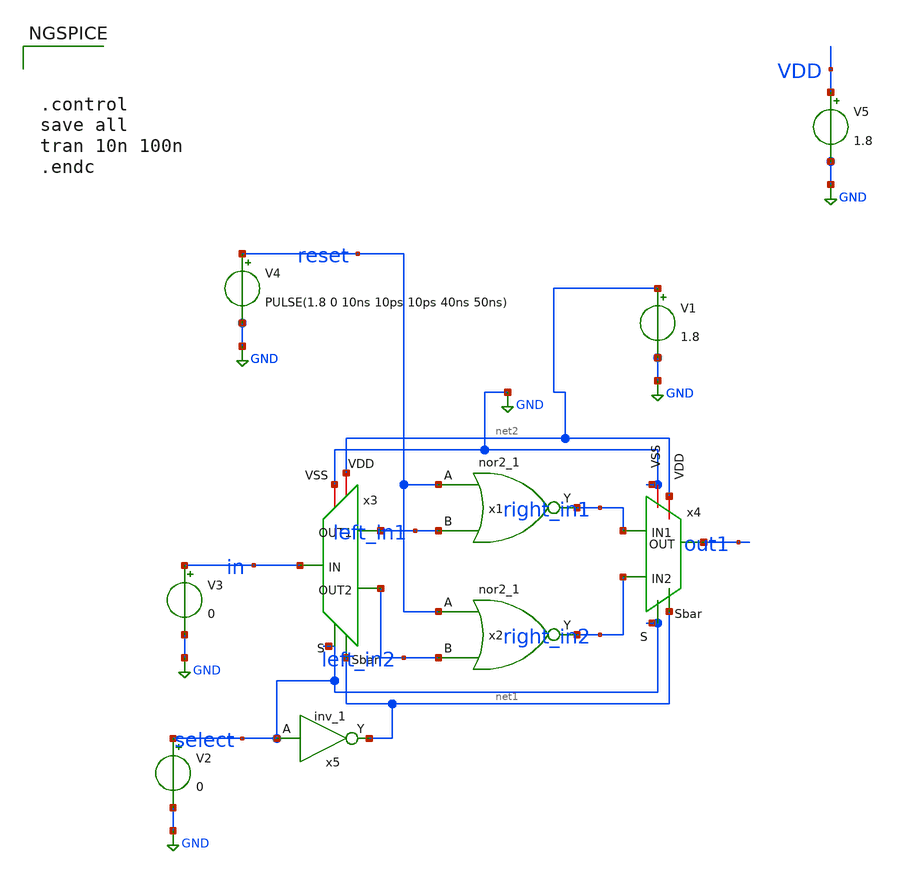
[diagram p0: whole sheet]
** sch_path: xiaolin/singlestage_tb.sch
**.subckt singlestage_tb
x1 reset left_in1 GND GND VDD VDD right_in1 sky130_fd_sc_hd__nor2_1
x2 reset left_in2 GND GND VDD VDD right_in2 sky130_fd_sc_hd__nor2_1
x3 select GND left_in1 net2 in net1 left_in2 demux2-1
x4 select GND right_in1 net2 out1 net1 right_in2 mux2-1
x5 select GND GND VDD VDD net1 sky130_fd_sc_hd__inv_1
V1 net2 GND 1.8
V2 select GND 0
V3 in GND 0
V4 reset GND PULSE(1.8 0 10ns 10ps 10ps 40ns 50ns)
V5 VDD GND 1.8
**** begin user architecture code

** opencircuitdesign pdks install
*.lib /farmshare/home/classes/ee/372/PDKs/open_pdks/sky130/sky130A/libs.tech/ngspice/sky130.lib.spice mc
.lib ~/372puf/ee372/sky130A/libs.tech/ngspice/sky130.lib.spice mc
.include /farmshare/home/classes/ee/372/PDKs/open_pdks/sky130/sky130A/libs.ref/sky130_fd_sc_hd/spice/sky130_fd_sc_hd.spice






.control
save all
tran 10n 100n
.endc


**** end user architecture code
**.ends

* expanding   symbol:  demux2-1.sym # of pins=7
** sym_path: xiaolin/demux2-1.sym
** sch_path: xiaolin/demux2-1.sch
.subckt demux2-1 S VSS OUT1 VDD IN Sbar OUT2
*.ipin Sbar
*.ipin S
*.iopin VSS
*.iopin VDD
*.opin OUT1
*.opin OUT2
*.ipin IN
XM2 IN S OUT1 VSS sky130_fd_pr__nfet_01v8 L=0.15 W=0.65 nf=1 ad='int((nf+1)/2) * W/nf * 0.29' as='int((nf+2)/2) * W/nf * 0.29'
+ pd='2*int((nf+1)/2) * (W/nf + 0.29)' ps='2*int((nf+2)/2) * (W/nf + 0.29)' nrd='0.29 / W' nrs='0.29 / W'
+ sa=0 sb=0 sd=0 mult=1 m=1
XM1 IN Sbar OUT2 VSS sky130_fd_pr__nfet_01v8 L=0.15 W=0.65 nf=1 ad='int((nf+1)/2) * W/nf * 0.29' as='int((nf+2)/2) * W/nf * 0.29'
+ pd='2*int((nf+1)/2) * (W/nf + 0.29)' ps='2*int((nf+2)/2) * (W/nf + 0.29)' nrd='0.29 / W' nrs='0.29 / W'
+ sa=0 sb=0 sd=0 mult=1 m=1
XM3 IN S OUT2 VDD sky130_fd_pr__pfet_01v8_hvt L=0.15 W=1 nf=1 ad='int((nf+1)/2) * W/nf * 0.29' as='int((nf+2)/2) * W/nf * 0.29'
+ pd='2*int((nf+1)/2) * (W/nf + 0.29)' ps='2*int((nf+2)/2) * (W/nf + 0.29)' nrd='0.29 / W' nrs='0.29 / W'
+ sa=0 sb=0 sd=0 mult=1 m=1
XM4 IN Sbar OUT1 VDD sky130_fd_pr__pfet_01v8_hvt L=0.15 W=1 nf=1 ad='int((nf+1)/2) * W/nf * 0.29' as='int((nf+2)/2) * W/nf * 0.29'
+ pd='2*int((nf+1)/2) * (W/nf + 0.29)' ps='2*int((nf+2)/2) * (W/nf + 0.29)' nrd='0.29 / W' nrs='0.29 / W'
+ sa=0 sb=0 sd=0 mult=1 m=1
XM5 IN S OUT2 VDD sky130_fd_pr__pfet_01v8_hvt L=0.15 W=1 nf=1 ad='int((nf+1)/2) * W/nf * 0.29' as='int((nf+2)/2) * W/nf * 0.29'
+ pd='2*int((nf+1)/2) * (W/nf + 0.29)' ps='2*int((nf+2)/2) * (W/nf + 0.29)' nrd='0.29 / W' nrs='0.29 / W'
+ sa=0 sb=0 sd=0 mult=1 m=1
.ends


* expanding   symbol:  mux2-1.sym # of pins=7
** sym_path: design/mux2-1.sym
** sch_path: design/mux2-1.sch
.subckt mux2-1 S VSS IN1 VDD OUT Sbar IN2
*.ipin IN1
*.ipin IN2
*.ipin Sbar
*.ipin S
*.opin OUT
*.iopin VSS
*.iopin VDD
XM2 IN1 S OUT VSS sky130_fd_pr__nfet_01v8 L=0.15 W=0.65 nf=1 ad='int((nf+1)/2) * W/nf * 0.29' as='int((nf+2)/2) * W/nf * 0.29'
+ pd='2*int((nf+1)/2) * (W/nf + 0.29)' ps='2*int((nf+2)/2) * (W/nf + 0.29)' nrd='0.29 / W' nrs='0.29 / W'
+ sa=0 sb=0 sd=0 mult=1 m=1
XM1 IN2 Sbar OUT VSS sky130_fd_pr__nfet_01v8 L=0.15 W=0.65 nf=1 ad='int((nf+1)/2) * W/nf * 0.29' as='int((nf+2)/2) * W/nf * 0.29'
+ pd='2*int((nf+1)/2) * (W/nf + 0.29)' ps='2*int((nf+2)/2) * (W/nf + 0.29)' nrd='0.29 / W' nrs='0.29 / W'
+ sa=0 sb=0 sd=0 mult=1 m=1
XM4 IN1 Sbar OUT VDD sky130_fd_pr__pfet_01v8_hvt L=0.15 W=1 nf=1 ad='int((nf+1)/2) * W/nf * 0.29' as='int((nf+2)/2) * W/nf * 0.29'
+ pd='2*int((nf+1)/2) * (W/nf + 0.29)' ps='2*int((nf+2)/2) * (W/nf + 0.29)' nrd='0.29 / W' nrs='0.29 / W'
+ sa=0 sb=0 sd=0 mult=1 m=1
XM5 IN2 S OUT VDD sky130_fd_pr__pfet_01v8_hvt L=0.15 W=1 nf=1 ad='int((nf+1)/2) * W/nf * 0.29' as='int((nf+2)/2) * W/nf * 0.29'
+ pd='2*int((nf+1)/2) * (W/nf + 0.29)' ps='2*int((nf+2)/2) * (W/nf + 0.29)' nrd='0.29 / W' nrs='0.29 / W'
+ sa=0 sb=0 sd=0 mult=1 m=1
.ends

.GLOBAL GND
.end
